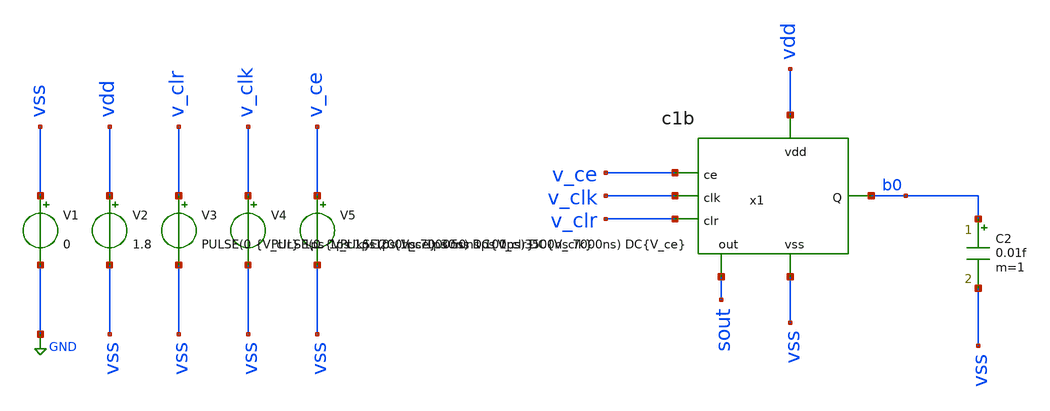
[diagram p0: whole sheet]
** sch_path: track_vlsi/martinez-sapriza/sch/tb_c1b.sch
**.subckt tb_c1b
V1 vss GND 0
V2 vdd vss 1.8
V3 v_clr vss PULSE(0 {V_clr} 1ps 1ps 1ps 200ns 7000ns) DC{V_clr}
V4 v_clk vss PULSE(0 {V_clk} 1ps 1ps 1ps 50ns 100ns) DC{V_clk}
V5 v_ce vss PULSE(0 {V_ce} 30ns 1ps 1ps 3500ns 7000ns) DC{V_ce}
C2 b0 vss 0.01f m=1
x1 v_ce v_clk v_clr vdd vss b0 sout c1b
**** begin user architecture code



* Circuit parameters
.param V_clk = 1.8
.param V_clr = 1.8
.param V_ce = 1.8
.options TEMP = 27.0

* Include
.lib /home/eamta/skywater/skywater-pdk/libraries/sky130_fd_pr_ngspice/latest/models/corners/sky130.lib TT

* Signals to save
.save all

* Simulation
.control
  tran 10n 700ns
  setplot tran1
  plot v(v_clr) v(v_clk) v(v_ce)
  write tb_c1b_tran1.raw

  tran 10n 700ns
  setplot tran2
  plot v(b0)
  write tb_c1b_tran2.raw

.endc

.end



**** end user architecture code
**.ends
.GLOBAL GND
.end
